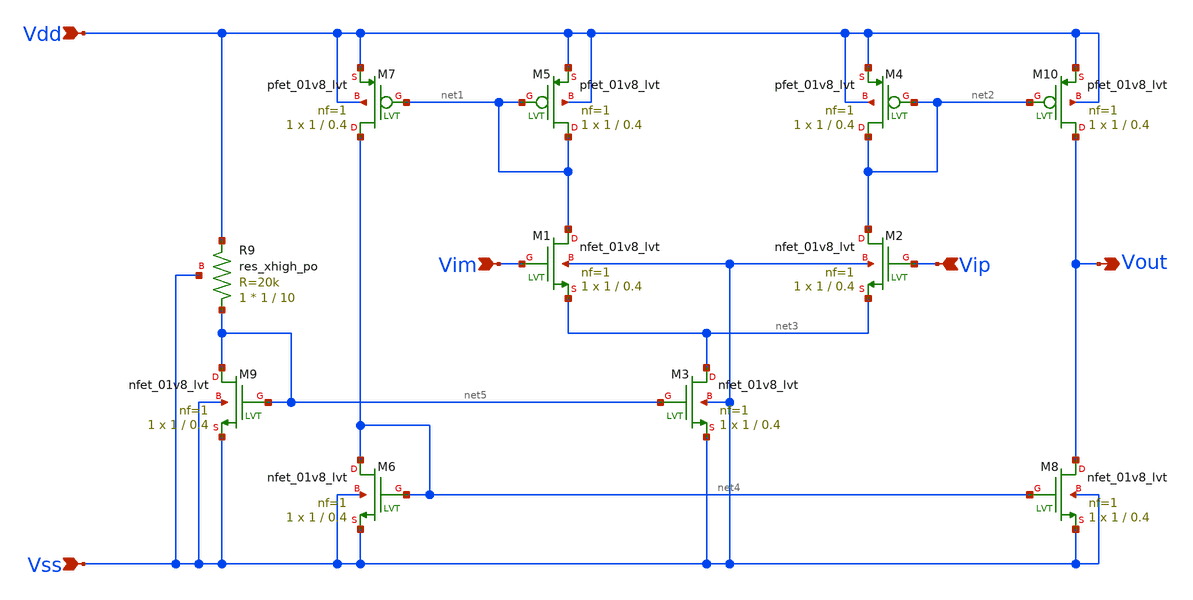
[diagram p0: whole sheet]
** sch_path: schematic/ota_n_selfbias.sch
**.subckt ota_n_selfbias Vim Vip Vout Vdd Vss
*.ipin Vim
*.ipin Vip
*.opin Vout
*.ipin Vdd
*.ipin Vss
XM1 net1 Vim net3 Vss sky130_fd_pr__nfet_01v8_lvt L=0.4 W=1 nf=1 ad='int((1 + 1)/2) * 1 / 1 * 0.29' as='int((1 + 2)/2) * 1 / 1 * 0.29'
+ pd='2*int((1 + 1)/2) * (1 / 1 + 0.29)' ps='2*int((1 + 2)/2) * (1 / 1 + 0.29)' nrd='0.29 / 1 ' nrs='0.29 / 1 '
+ sa=0 sb=0 sd=0 mult=1 m=1
XM2 net2 Vip net3 Vss sky130_fd_pr__nfet_01v8_lvt L=0.4 W=1 nf=1 ad='int((1 + 1)/2) * 1 / 1 * 0.29' as='int((1 + 2)/2) * 1 / 1 * 0.29'
+ pd='2*int((1 + 1)/2) * (1 / 1 + 0.29)' ps='2*int((1 + 2)/2) * (1 / 1 + 0.29)' nrd='0.29 / 1 ' nrs='0.29 / 1 '
+ sa=0 sb=0 sd=0 mult=1 m=1
XM3 net3 net5 Vss Vss sky130_fd_pr__nfet_01v8_lvt L=0.4 W=1 nf=1 ad='int((1 + 1)/2) * 1 / 1 * 0.29' as='int((1 + 2)/2) * 1 / 1 * 0.29'
+ pd='2*int((1 + 1)/2) * (1 / 1 + 0.29)' ps='2*int((1 + 2)/2) * (1 / 1 + 0.29)' nrd='0.29 / 1 ' nrs='0.29 / 1 '
+ sa=0 sb=0 sd=0 mult=1 m=1
XM10 Vout net2 Vdd Vdd sky130_fd_pr__pfet_01v8_lvt L=0.4 W=1 nf=1 ad='int((1 + 1)/2) * 1 / 1 * 0.29'
+ as='int((1 + 2)/2) * 1 / 1 * 0.29' pd='2*int((1 + 1)/2) * (1 / 1 + 0.29)' ps='2*int((1 + 2)/2) * (1 / 1 + 0.29)'
+ nrd='0.29 / 1 ' nrs='0.29 / 1 ' sa=0 sb=0 sd=0 mult=1 m=1
XM4 net2 net2 Vdd Vdd sky130_fd_pr__pfet_01v8_lvt L=0.4 W=1 nf=1 ad='int((1 + 1)/2) * 1 / 1 * 0.29' as='int((1 + 2)/2) * 1 / 1 * 0.29'
+ pd='2*int((1 + 1)/2) * (1 / 1 + 0.29)' ps='2*int((1 + 2)/2) * (1 / 1 + 0.29)' nrd='0.29 / 1 ' nrs='0.29 / 1 '
+ sa=0 sb=0 sd=0 mult=1 m=1
XM5 net1 net1 Vdd Vdd sky130_fd_pr__pfet_01v8_lvt L=0.4 W=1 nf=1 ad='int((1 + 1)/2) * 1 / 1 * 0.29' as='int((1 + 2)/2) * 1 / 1 * 0.29'
+ pd='2*int((1 + 1)/2) * (1 / 1 + 0.29)' ps='2*int((1 + 2)/2) * (1 / 1 + 0.29)' nrd='0.29 / 1 ' nrs='0.29 / 1 '
+ sa=0 sb=0 sd=0 mult=1 m=1
XM7 net4 net1 Vdd Vdd sky130_fd_pr__pfet_01v8_lvt L=0.4 W=1 nf=1 ad='int((1 + 1)/2) * 1 / 1 * 0.29' as='int((1 + 2)/2) * 1 / 1 * 0.29'
+ pd='2*int((1 + 1)/2) * (1 / 1 + 0.29)' ps='2*int((1 + 2)/2) * (1 / 1 + 0.29)' nrd='0.29 / 1 ' nrs='0.29 / 1 '
+ sa=0 sb=0 sd=0 mult=1 m=1
XM6 net4 net4 Vss Vss sky130_fd_pr__nfet_01v8_lvt L=0.4 W=1 nf=1 ad='int((1 + 1)/2) * 1 / 1 * 0.29' as='int((1 + 2)/2) * 1 / 1 * 0.29'
+ pd='2*int((1 + 1)/2) * (1 / 1 + 0.29)' ps='2*int((1 + 2)/2) * (1 / 1 + 0.29)' nrd='0.29 / 1 ' nrs='0.29 / 1 '
+ sa=0 sb=0 sd=0 mult=1 m=1
XM8 Vout net4 Vss Vss sky130_fd_pr__nfet_01v8_lvt L=0.4 W=1 nf=1 ad='int((1 + 1)/2) * 1 / 1 * 0.29' as='int((1 + 2)/2) * 1 / 1 * 0.29'
+ pd='2*int((1 + 1)/2) * (1 / 1 + 0.29)' ps='2*int((1 + 2)/2) * (1 / 1 + 0.29)' nrd='0.29 / 1 ' nrs='0.29 / 1 '
+ sa=0 sb=0 sd=0 mult=1 m=1
XM9 net5 net5 Vss Vss sky130_fd_pr__nfet_01v8_lvt L=0.4 W=1 nf=1 ad='int((1 + 1)/2) * 1 / 1 * 0.29' as='int((1 + 2)/2) * 1 / 1 * 0.29'
+ pd='2*int((1 + 1)/2) * (1 / 1 + 0.29)' ps='2*int((1 + 2)/2) * (1 / 1 + 0.29)' nrd='0.29 / 1 ' nrs='0.29 / 1 '
+ sa=0 sb=0 sd=0 mult=1 m=1
XR9 net5 Vdd Vss sky130_fd_pr__res_xhigh_po W=1 L=10 mult=1 m=1
**.ends
.end
